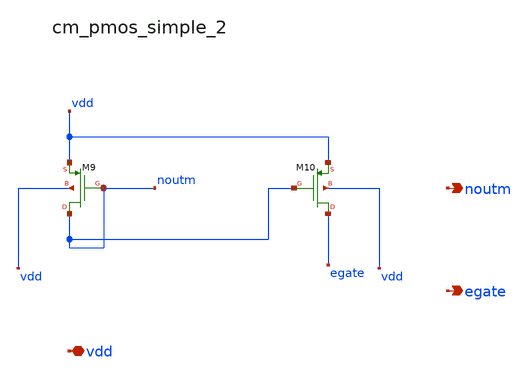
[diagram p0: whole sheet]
** sch_path: analog-db/raw/ldo_005_buffered_ref/hier/blocks/cm_pmos_simple_2.sch
**.subckt cm_pmos_simple_2 vdd noutm egate
*.iopin vdd
*.opin noutm
*.opin egate
XM10 egate noutm vdd vdd sg13_lv_pmos w=x_dut_xm10_w l=x_dut_xm10_l ng=1 m=1
XM9 noutm noutm vdd vdd sg13_lv_pmos w=x_dut_xm9_w l=x_dut_xm9_l ng=1 m=1
**.ends
.end
